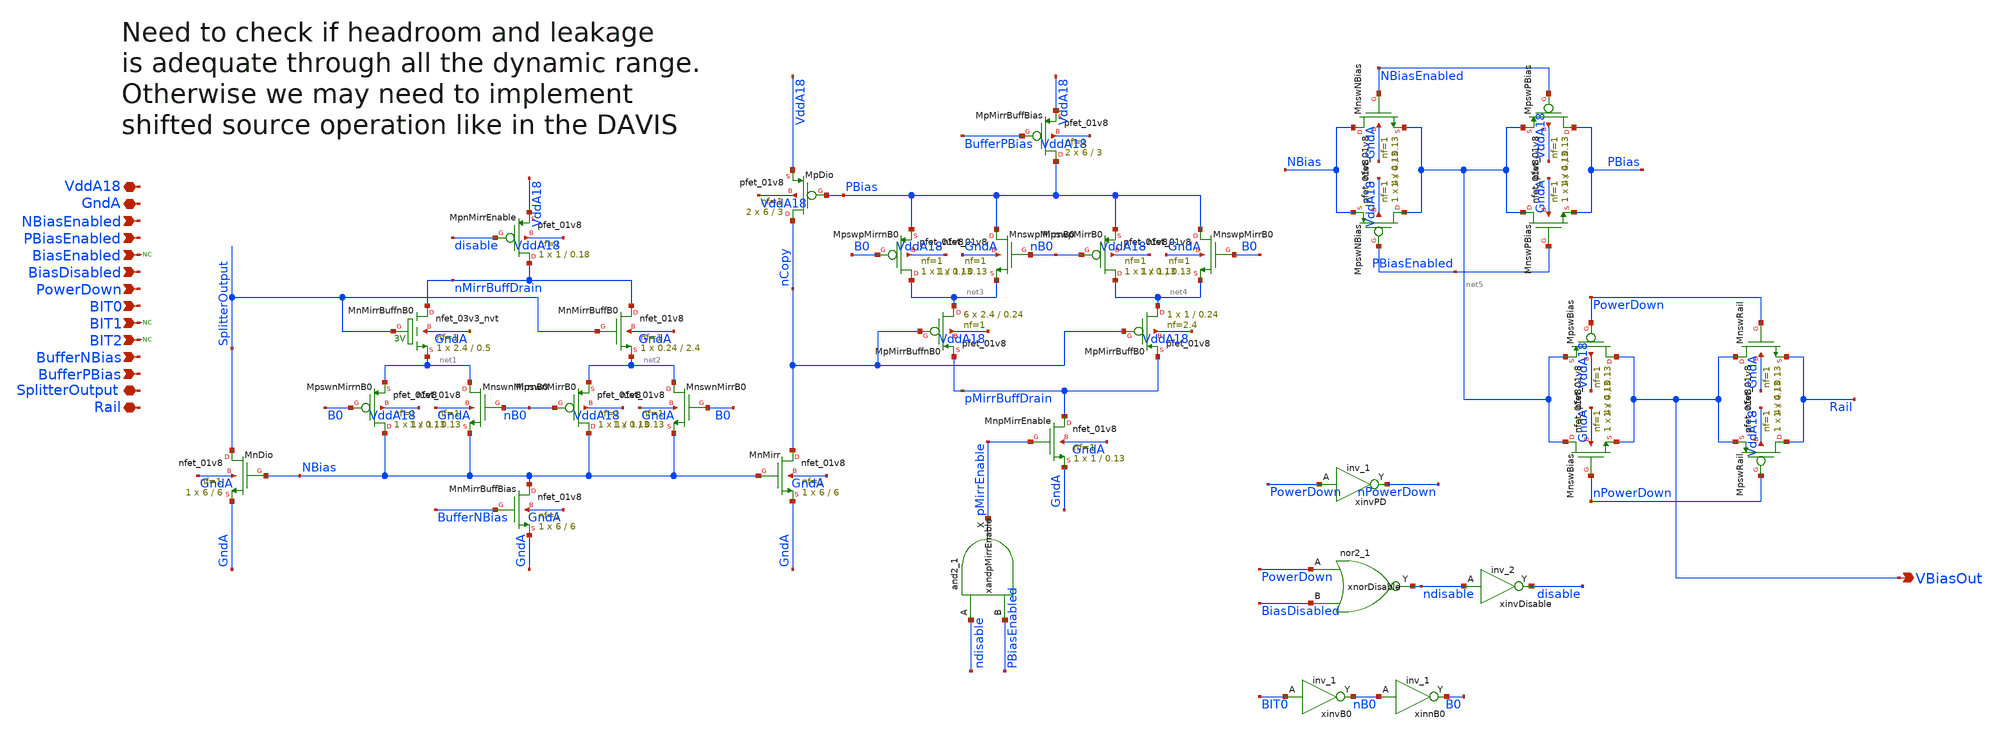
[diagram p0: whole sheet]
** sch_path: analog/xschem/BiasBuffers.sch
**.subckt BiasBuffers GndA VddA18 VBiasOut NBiasEnabled PBiasEnabled BiasEnabled BiasDisabled
*+ PowerDown BIT0 BIT1 BIT2 BufferNBias BufferPBias SplitterOutput Rail
*.iopin GndA
*.iopin VddA18
*.opin VBiasOut
*.ipin NBiasEnabled
*.ipin PBiasEnabled
*.ipin BiasEnabled
*.ipin BiasDisabled
*.ipin PowerDown
*.ipin BIT0
*.ipin BIT1
*.ipin BIT2
*.ipin BufferNBias
*.ipin BufferPBias
*.iopin SplitterOutput
*.iopin Rail
XMnDio SplitterOutput NBias GndA GndA sky130_fd_pr__nfet_01v8 L=6 W=6 nf=1 ad='int((1 + 1)/2) * 6 / 1 * 0.29'
+ as='int((1 + 2)/2) * 6 / 1 * 0.29' pd='2*int((1 + 1)/2) * (6 / 1 + 0.29)' ps='2*int((1 + 2)/2) * (6 / 1 + 0.29)'
+ nrd='0.29 / 6 ' nrs='0.29 / 6 ' sa=0 sb=0 sd=0 mult=1 m=1
XMnswnMirrnB0 net1 nB0 NBias GndA sky130_fd_pr__nfet_01v8 L=0.13 W=1 nf=1 ad='int((1 + 1)/2) * 1 / 1 * 0.29'
+ as='int((1 + 2)/2) * 1 / 1 * 0.29' pd='2*int((1 + 1)/2) * (1 / 1 + 0.29)' ps='2*int((1 + 2)/2) * (1 / 1 + 0.29)'
+ nrd='0.29 / 1 ' nrs='0.29 / 1 ' sa=0 sb=0 sd=0 mult=1 m=1
XMpswnMirrnB0 NBias B0 net1 VddA18 sky130_fd_pr__pfet_01v8 L=0.13 W=1 nf=1 ad='int((1 + 1)/2) * 1 / 1 * 0.29'
+ as='int((1 + 2)/2) * 1 / 1 * 0.29' pd='2*int((1 + 1)/2) * (1 / 1 + 0.29)' ps='2*int((1 + 2)/2) * (1 / 1 + 0.29)'
+ nrd='0.29 / 1 ' nrs='0.29 / 1 ' sa=0 sb=0 sd=0 mult=1 m=1
XMnMirrBuffnB0 nMirrBuffDrain SplitterOutput net1 GndA sky130_fd_pr__nfet_03v3_nvt L=0.5 W=2.4 nf=1 ad='int((1 + 1)/2) * 2.4 / 1 * 0.29'
+ as='int((1 + 2)/2) * 2.4 / 1 * 0.29' pd='2*int((1 + 1)/2) * (2.4 / 1 + 0.29)' ps='2*int((1 + 2)/2) * (2.4 / 1 + 0.29)'
+ nrd='0.29 / 2.4 ' nrs='0.29 / 2.4 ' sa=0 sb=0 sd=0 mult=1 m=1
XMnMirrBuffB0 nMirrBuffDrain SplitterOutput net2 GndA sky130_fd_pr__nfet_01v8 L=2.4 W=0.24 nf=1 ad='int((1 + 1)/2) * 0.24 / 1 * 0.29'
+ as='int((1 + 2)/2) * 0.24 / 1 * 0.29' pd='2*int((1 + 1)/2) * (0.24 / 1 + 0.29)' ps='2*int((1 + 2)/2) * (0.24 / 1 + 0.29)'
+ nrd='0.29 / 0.24 ' nrs='0.29 / 0.24 ' sa=0 sb=0 sd=0 mult=1 m=1
XMpnMirrEnable nMirrBuffDrain disable VddA18 VddA18 sky130_fd_pr__pfet_01v8 L=0.18 W=1 nf=1 ad='int((1 + 1)/2) * 1 / 1 * 0.29'
+ as='int((1 + 2)/2) * 1 / 1 * 0.29' pd='2*int((1 + 1)/2) * (1 / 1 + 0.29)' ps='2*int((1 + 2)/2) * (1 / 1 + 0.29)'
+ nrd='0.29 / 1 ' nrs='0.29 / 1 ' sa=0 sb=0 sd=0 mult=1 m=1
XMnswnMirrB0 net2 B0 NBias GndA sky130_fd_pr__nfet_01v8 L=0.13 W=1 nf=1 ad='int((1 + 1)/2) * 1 / 1 * 0.29'
+ as='int((1 + 2)/2) * 1 / 1 * 0.29' pd='2*int((1 + 1)/2) * (1 / 1 + 0.29)' ps='2*int((1 + 2)/2) * (1 / 1 + 0.29)'
+ nrd='0.29 / 1 ' nrs='0.29 / 1 ' sa=0 sb=0 sd=0 mult=1 m=1
XMpswnMirrB0 NBias nB0 net2 VddA18 sky130_fd_pr__pfet_01v8 L=0.13 W=1 nf=1 ad='int((1 + 1)/2) * 1 / 1 * 0.29'
+ as='int((1 + 2)/2) * 1 / 1 * 0.29' pd='2*int((1 + 1)/2) * (1 / 1 + 0.29)' ps='2*int((1 + 2)/2) * (1 / 1 + 0.29)'
+ nrd='0.29 / 1 ' nrs='0.29 / 1 ' sa=0 sb=0 sd=0 mult=1 m=1
XMnMirr nCopy NBias GndA GndA sky130_fd_pr__nfet_01v8 L=6 W=6 nf=1 ad='int((1 + 1)/2) * 6 / 1 * 0.29'
+ as='int((1 + 2)/2) * 6 / 1 * 0.29' pd='2*int((1 + 1)/2) * (6 / 1 + 0.29)' ps='2*int((1 + 2)/2) * (6 / 1 + 0.29)'
+ nrd='0.29 / 6 ' nrs='0.29 / 6 ' sa=0 sb=0 sd=0 mult=1 m=1
XMnMirrBuffBias NBias BufferNBias GndA GndA sky130_fd_pr__nfet_01v8 L=6 W=6 nf=1 ad='int((1 + 1)/2) * 6 / 1 * 0.29'
+ as='int((1 + 2)/2) * 6 / 1 * 0.29' pd='2*int((1 + 1)/2) * (6 / 1 + 0.29)' ps='2*int((1 + 2)/2) * (6 / 1 + 0.29)'
+ nrd='0.29 / 6 ' nrs='0.29 / 6 ' sa=0 sb=0 sd=0 mult=1 m=1
XMpDio nCopy PBias VddA18 VddA18 sky130_fd_pr__pfet_01v8 L=3 W=6 nf=1 ad='int((1 + 1)/2) * 6 / 1 * 0.29'
+ as='int((1 + 2)/2) * 6 / 1 * 0.29' pd='2*int((1 + 1)/2) * (6 / 1 + 0.29)' ps='2*int((1 + 2)/2) * (6 / 1 + 0.29)'
+ nrd='0.29 / 6 ' nrs='0.29 / 6 ' sa=0 sb=0 sd=0 mult=2 m=2
XMnswpMirrnB0 PBias nB0 net3 GndA sky130_fd_pr__nfet_01v8 L=0.13 W=1 nf=1 ad='int((1 + 1)/2) * 1 / 1 * 0.29'
+ as='int((1 + 2)/2) * 1 / 1 * 0.29' pd='2*int((1 + 1)/2) * (1 / 1 + 0.29)' ps='2*int((1 + 2)/2) * (1 / 1 + 0.29)'
+ nrd='0.29 / 1 ' nrs='0.29 / 1 ' sa=0 sb=0 sd=0 mult=1 m=1
XMpswpMirrnB0 net3 B0 PBias VddA18 sky130_fd_pr__pfet_01v8 L=0.13 W=1 nf=1 ad='int((1 + 1)/2) * 1 / 1 * 0.29'
+ as='int((1 + 2)/2) * 1 / 1 * 0.29' pd='2*int((1 + 1)/2) * (1 / 1 + 0.29)' ps='2*int((1 + 2)/2) * (1 / 1 + 0.29)'
+ nrd='0.29 / 1 ' nrs='0.29 / 1 ' sa=0 sb=0 sd=0 mult=1 m=1
XMnswpMirrB0 PBias B0 net4 GndA sky130_fd_pr__nfet_01v8 L=0.13 W=1 nf=1 ad='int((1 + 1)/2) * 1 / 1 * 0.29'
+ as='int((1 + 2)/2) * 1 / 1 * 0.29' pd='2*int((1 + 1)/2) * (1 / 1 + 0.29)' ps='2*int((1 + 2)/2) * (1 / 1 + 0.29)'
+ nrd='0.29 / 1 ' nrs='0.29 / 1 ' sa=0 sb=0 sd=0 mult=1 m=1
XMpswpMirrB0 net4 nB0 PBias VddA18 sky130_fd_pr__pfet_01v8 L=0.13 W=1 nf=1 ad='int((1 + 1)/2) * 1 / 1 * 0.29'
+ as='int((1 + 2)/2) * 1 / 1 * 0.29' pd='2*int((1 + 1)/2) * (1 / 1 + 0.29)' ps='2*int((1 + 2)/2) * (1 / 1 + 0.29)'
+ nrd='0.29 / 1 ' nrs='0.29 / 1 ' sa=0 sb=0 sd=0 mult=1 m=1
XMpMirrBuffnB0 net3 nCopy pMirrBuffDrain VddA18 sky130_fd_pr__pfet_01v8 L=0.24 W=2.4 nf=1 ad='int((1 + 1)/2) * 2.4 / 1 * 0.29'
+ as='int((1 + 2)/2) * 2.4 / 1 * 0.29' pd='2*int((1 + 1)/2) * (2.4 / 1 + 0.29)' ps='2*int((1 + 2)/2) * (2.4 / 1 + 0.29)'
+ nrd='0.29 / 2.4 ' nrs='0.29 / 2.4 ' sa=0 sb=0 sd=0 mult=6 m=6
XMpMirrBuffB0 net4 nCopy pMirrBuffDrain VddA18 sky130_fd_pr__pfet_01v8 L=0.24 W=1 nf=2.4 ad='int((2.4 + 1)/2) * 1 / 2.4 * 0.29'
+ as='int((2.4 + 2)/2) * 1 / 2.4 * 0.29' pd='2*int((2.4 + 1)/2) * (1 / 2.4 + 0.29)' ps='2*int((2.4 + 2)/2) * (1 / 2.4 + 0.29)'
+ nrd='0.29 / 1 ' nrs='0.29 / 1 ' sa=0 sb=0 sd=0 mult=1 m=1
XMnpMirrEnable pMirrBuffDrain pMirrEnable GndA GndA sky130_fd_pr__nfet_01v8 L=0.13 W=1 nf=1 ad='int((1 + 1)/2) * 1 / 1 * 0.29'
+ as='int((1 + 2)/2) * 1 / 1 * 0.29' pd='2*int((1 + 1)/2) * (1 / 1 + 0.29)' ps='2*int((1 + 2)/2) * (1 / 1 + 0.29)'
+ nrd='0.29 / 1 ' nrs='0.29 / 1 ' sa=0 sb=0 sd=0 mult=1 m=1
xandpMirrEnable ndisable PBiasEnabled GndA GndA VddA18 VddA18 pMirrEnable sky130_fd_sc_hd__and2_1
XMpMirrBuffBias PBias BufferPBias VddA18 VddA18 sky130_fd_pr__pfet_01v8 L=3 W=6 nf=1 ad='int((1 + 1)/2) * 6 / 1 * 0.29'
+ as='int((1 + 2)/2) * 6 / 1 * 0.29' pd='2*int((1 + 1)/2) * (6 / 1 + 0.29)' ps='2*int((1 + 2)/2) * (6 / 1 + 0.29)'
+ nrd='0.29 / 6 ' nrs='0.29 / 6 ' sa=0 sb=0 sd=0 mult=2 m=2
xnorDisable PowerDown BiasDisabled GndA GndA VddA18 VddA18 ndisable sky130_fd_sc_hd__nor2_1
xinvDisable ndisable GndA GndA VddA18 VddA18 disable sky130_fd_sc_hd__inv_2
XMnswNBias NBias NBiasEnabled net5 GndA sky130_fd_pr__nfet_01v8 L=0.13 W=4 nf=1 ad='int((1 + 1)/2) * 4 / 1 * 0.29'
+ as='int((1 + 2)/2) * 4 / 1 * 0.29' pd='2*int((1 + 1)/2) * (4 / 1 + 0.29)' ps='2*int((1 + 2)/2) * (4 / 1 + 0.29)'
+ nrd='0.29 / 4 ' nrs='0.29 / 4 ' sa=0 sb=0 sd=0 mult=1 m=1
XMpswNBias net5 PBiasEnabled NBias VddA18 sky130_fd_pr__pfet_01v8 L=0.13 W=4 nf=1 ad='int((1 + 1)/2) * 4 / 1 * 0.29'
+ as='int((1 + 2)/2) * 4 / 1 * 0.29' pd='2*int((1 + 1)/2) * (4 / 1 + 0.29)' ps='2*int((1 + 2)/2) * (4 / 1 + 0.29)'
+ nrd='0.29 / 4 ' nrs='0.29 / 4 ' sa=0 sb=0 sd=0 mult=1 m=1
XMnswPBias net5 PBiasEnabled PBias GndA sky130_fd_pr__nfet_01v8 L=0.13 W=4 nf=1 ad='int((1 + 1)/2) * 4 / 1 * 0.29'
+ as='int((1 + 2)/2) * 4 / 1 * 0.29' pd='2*int((1 + 1)/2) * (4 / 1 + 0.29)' ps='2*int((1 + 2)/2) * (4 / 1 + 0.29)'
+ nrd='0.29 / 4 ' nrs='0.29 / 4 ' sa=0 sb=0 sd=0 mult=1 m=1
XMpswPBias PBias NBiasEnabled net5 VddA18 sky130_fd_pr__pfet_01v8 L=0.13 W=4 nf=1 ad='int((1 + 1)/2) * 4 / 1 * 0.29'
+ as='int((1 + 2)/2) * 4 / 1 * 0.29' pd='2*int((1 + 1)/2) * (4 / 1 + 0.29)' ps='2*int((1 + 2)/2) * (4 / 1 + 0.29)'
+ nrd='0.29 / 4 ' nrs='0.29 / 4 ' sa=0 sb=0 sd=0 mult=1 m=1
XMnswBias net5 nPowerDown VBiasOut GndA sky130_fd_pr__nfet_01v8 L=0.13 W=4 nf=1 ad='int((1 + 1)/2) * 4 / 1 * 0.29'
+ as='int((1 + 2)/2) * 4 / 1 * 0.29' pd='2*int((1 + 1)/2) * (4 / 1 + 0.29)' ps='2*int((1 + 2)/2) * (4 / 1 + 0.29)'
+ nrd='0.29 / 4 ' nrs='0.29 / 4 ' sa=0 sb=0 sd=0 mult=1 m=1
XMpswBias VBiasOut PowerDown net5 VddA18 sky130_fd_pr__pfet_01v8 L=0.13 W=4 nf=1 ad='int((1 + 1)/2) * 4 / 1 * 0.29'
+ as='int((1 + 2)/2) * 4 / 1 * 0.29' pd='2*int((1 + 1)/2) * (4 / 1 + 0.29)' ps='2*int((1 + 2)/2) * (4 / 1 + 0.29)'
+ nrd='0.29 / 4 ' nrs='0.29 / 4 ' sa=0 sb=0 sd=0 mult=1 m=1
XMnswRail VBiasOut PowerDown Rail GndA sky130_fd_pr__nfet_01v8 L=0.13 W=4 nf=1 ad='int((1 + 1)/2) * 4 / 1 * 0.29'
+ as='int((1 + 2)/2) * 4 / 1 * 0.29' pd='2*int((1 + 1)/2) * (4 / 1 + 0.29)' ps='2*int((1 + 2)/2) * (4 / 1 + 0.29)'
+ nrd='0.29 / 4 ' nrs='0.29 / 4 ' sa=0 sb=0 sd=0 mult=1 m=1
XMpswRail Rail nPowerDown VBiasOut VddA18 sky130_fd_pr__pfet_01v8 L=0.13 W=4 nf=1 ad='int((1 + 1)/2) * 4 / 1 * 0.29'
+ as='int((1 + 2)/2) * 4 / 1 * 0.29' pd='2*int((1 + 1)/2) * (4 / 1 + 0.29)' ps='2*int((1 + 2)/2) * (4 / 1 + 0.29)'
+ nrd='0.29 / 4 ' nrs='0.29 / 4 ' sa=0 sb=0 sd=0 mult=1 m=1
xinvPD PowerDown GndA GndA VddA18 VddA18 nPowerDown sky130_fd_sc_hd__inv_1
xinvB0 BIT0 GndA GndA VddA18 VddA18 nB0 sky130_fd_sc_hd__inv_1
xinnB0 nB0 GndA GndA VddA18 VddA18 B0 sky130_fd_sc_hd__inv_1
* noconn BiasEnabled
* noconn BIT1
* noconn BIT2
**.ends
.end
